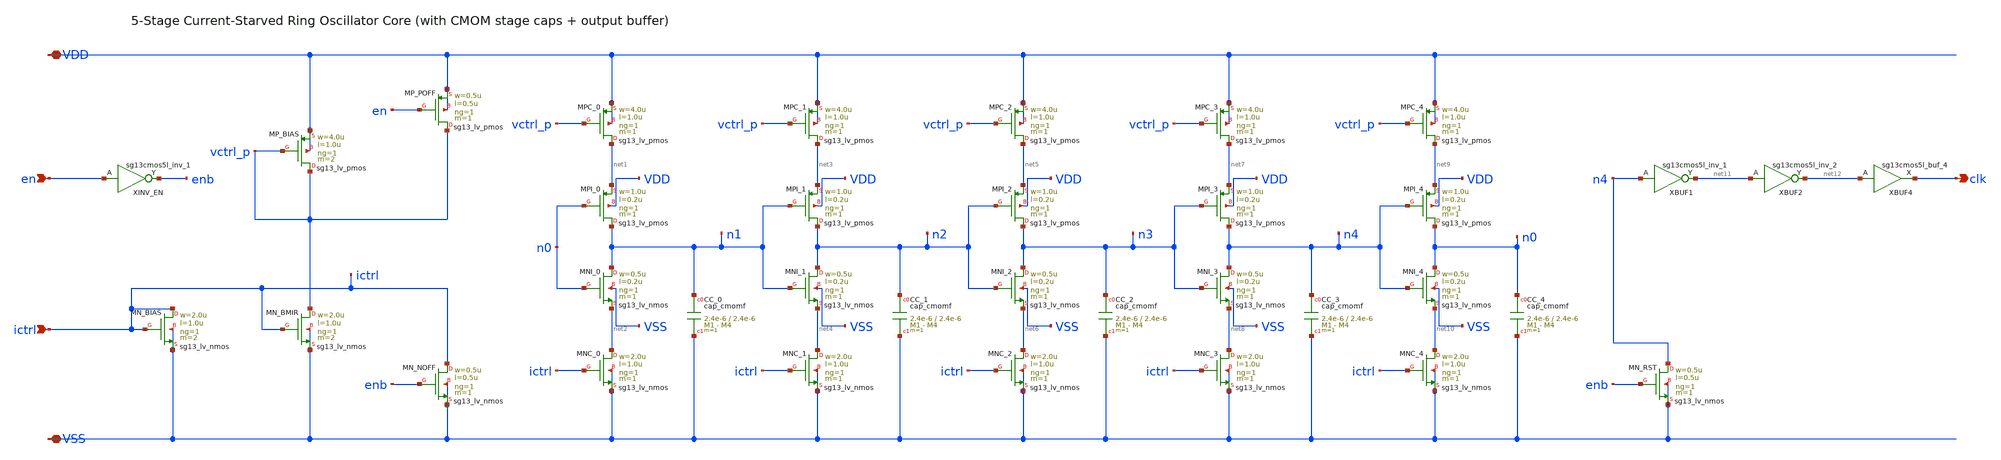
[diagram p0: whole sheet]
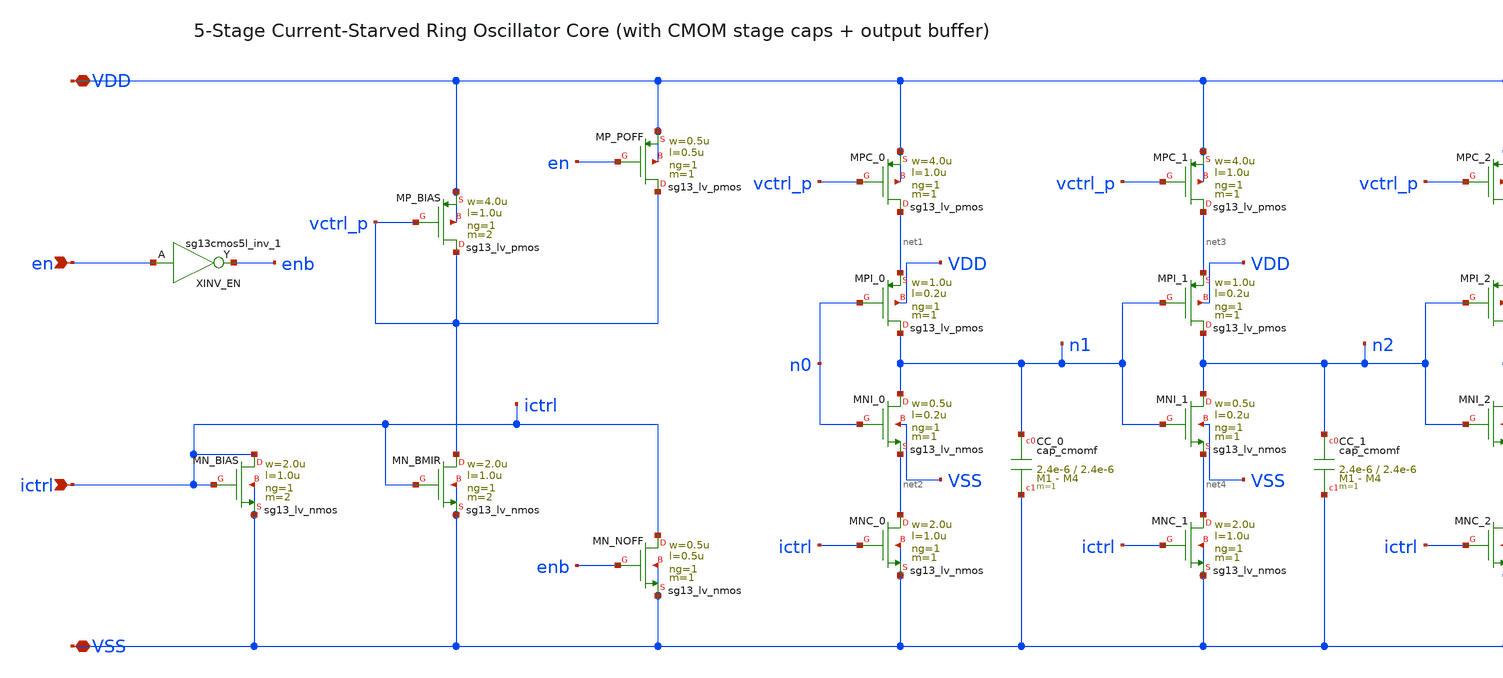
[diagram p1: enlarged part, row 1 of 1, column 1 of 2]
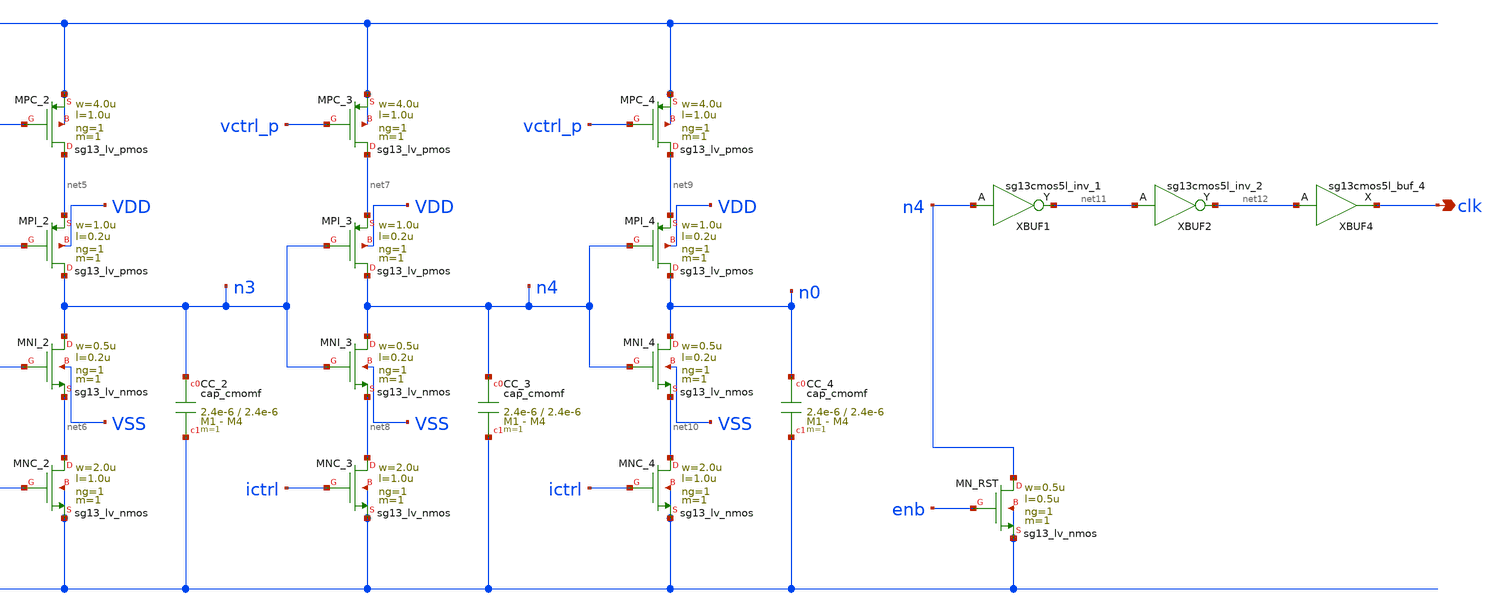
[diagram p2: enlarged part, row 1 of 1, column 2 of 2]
** sch_path: analog/osc_ring_cc/cco_core.sch
**.subckt cco_core VDD VSS en ictrl clk
*.iopin VDD
*.iopin VSS
*.ipin en
*.ipin ictrl
*.opin clk
XINV_EN enb en VDD VSS sg13cmos5l_inv_1
XMN_BIAS ictrl ictrl VSS VSS sg13_lv_nmos w=2.0u l=1.0u ng=1 m=2 mm_ok=1
XMP_BIAS vctrl_p vctrl_p VDD VDD sg13_lv_pmos w=4.0u l=1.0u ng=1 m=2 mm_ok=1
XMN_BMIR vctrl_p ictrl VSS VSS sg13_lv_nmos w=2.0u l=1.0u ng=1 m=2 mm_ok=1
XMP_POFF vctrl_p en VDD VDD sg13_lv_pmos w=0.5u l=0.5u ng=1 m=1 mm_ok=1
XMN_NOFF ictrl enb VSS VSS sg13_lv_nmos w=0.5u l=0.5u ng=1 m=1 mm_ok=1
XMPC_0 net1 vctrl_p VDD VDD sg13_lv_pmos w=4.0u l=1.0u ng=1 m=1 mm_ok=1
XMPI_0 n1 n0 net1 VDD sg13_lv_pmos w=1.0u l=0.2u ng=1 m=1 mm_ok=1
XMNI_0 n1 n0 net2 VSS sg13_lv_nmos w=0.5u l=0.2u ng=1 m=1 mm_ok=1
XMNC_0 net2 ictrl VSS VSS sg13_lv_nmos w=2.0u l=1.0u ng=1 m=1 mm_ok=1
XCC_0 n1 VSS cap_cmomf w=2.4e-6 l=2.4e-6 mmin=1 mmax=4 subblock=0 rfmodel=0 subscale=1 m=1 mm_ok=1
XMPC_1 net3 vctrl_p VDD VDD sg13_lv_pmos w=4.0u l=1.0u ng=1 m=1 mm_ok=1
XMPI_1 n2 n1 net3 VDD sg13_lv_pmos w=1.0u l=0.2u ng=1 m=1 mm_ok=1
XMNI_1 n2 n1 net4 VSS sg13_lv_nmos w=0.5u l=0.2u ng=1 m=1 mm_ok=1
XMNC_1 net4 ictrl VSS VSS sg13_lv_nmos w=2.0u l=1.0u ng=1 m=1 mm_ok=1
XCC_1 n2 VSS cap_cmomf w=2.4e-6 l=2.4e-6 mmin=1 mmax=4 subblock=0 rfmodel=0 subscale=1 m=1 mm_ok=1
XMPC_2 net5 vctrl_p VDD VDD sg13_lv_pmos w=4.0u l=1.0u ng=1 m=1 mm_ok=1
XMPI_2 n3 n2 net5 VDD sg13_lv_pmos w=1.0u l=0.2u ng=1 m=1 mm_ok=1
XMNI_2 n3 n2 net6 VSS sg13_lv_nmos w=0.5u l=0.2u ng=1 m=1 mm_ok=1
XMNC_2 net6 ictrl VSS VSS sg13_lv_nmos w=2.0u l=1.0u ng=1 m=1 mm_ok=1
XCC_2 n3 VSS cap_cmomf w=2.4e-6 l=2.4e-6 mmin=1 mmax=4 subblock=0 rfmodel=0 subscale=1 m=1 mm_ok=1
XMPC_3 net7 vctrl_p VDD VDD sg13_lv_pmos w=4.0u l=1.0u ng=1 m=1 mm_ok=1
XMPI_3 n4 n3 net7 VDD sg13_lv_pmos w=1.0u l=0.2u ng=1 m=1 mm_ok=1
XMNI_3 n4 n3 net8 VSS sg13_lv_nmos w=0.5u l=0.2u ng=1 m=1 mm_ok=1
XMNC_3 net8 ictrl VSS VSS sg13_lv_nmos w=2.0u l=1.0u ng=1 m=1 mm_ok=1
XCC_3 n4 VSS cap_cmomf w=2.4e-6 l=2.4e-6 mmin=1 mmax=4 subblock=0 rfmodel=0 subscale=1 m=1 mm_ok=1
XMPC_4 net9 vctrl_p VDD VDD sg13_lv_pmos w=4.0u l=1.0u ng=1 m=1 mm_ok=1
XMPI_4 n0 n4 net9 VDD sg13_lv_pmos w=1.0u l=0.2u ng=1 m=1 mm_ok=1
XMNI_4 n0 n4 net10 VSS sg13_lv_nmos w=0.5u l=0.2u ng=1 m=1 mm_ok=1
XMNC_4 net10 ictrl VSS VSS sg13_lv_nmos w=2.0u l=1.0u ng=1 m=1 mm_ok=1
XCC_4 n0 VSS cap_cmomf w=2.4e-6 l=2.4e-6 mmin=1 mmax=4 subblock=0 rfmodel=0 subscale=1 m=1 mm_ok=1
XMN_RST n4 enb VSS VSS sg13_lv_nmos w=0.5u l=0.5u ng=1 m=1 mm_ok=1
XBUF1 net11 n4 VDD VSS sg13cmos5l_inv_1
XBUF2 net12 net11 VDD VSS sg13cmos5l_inv_2
XBUF4 clk net12 VDD VSS sg13cmos5l_buf_4
**.ends
.end
